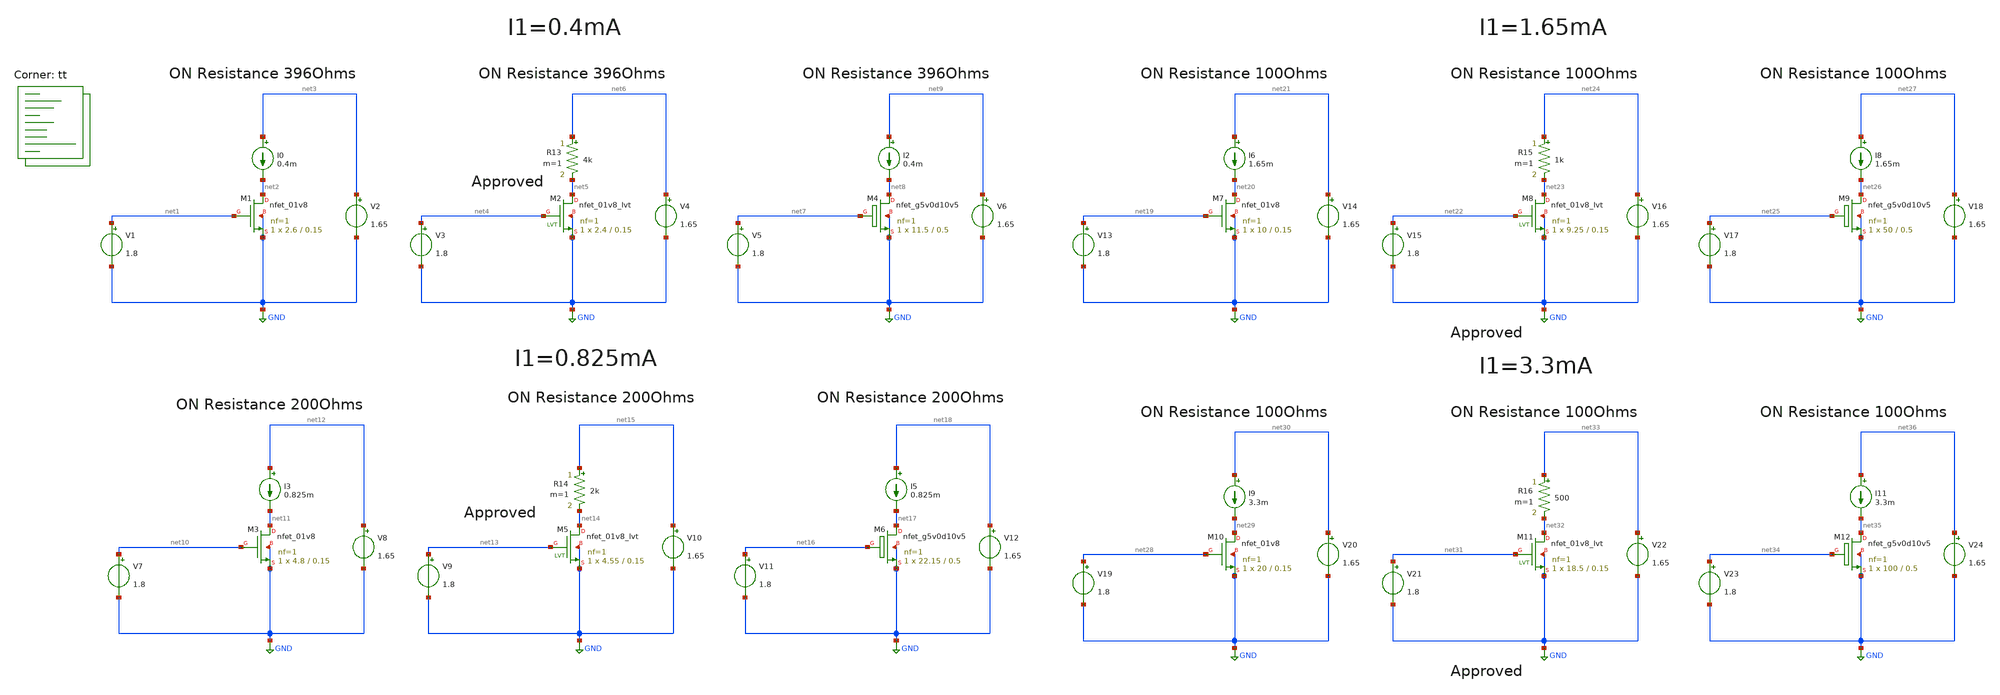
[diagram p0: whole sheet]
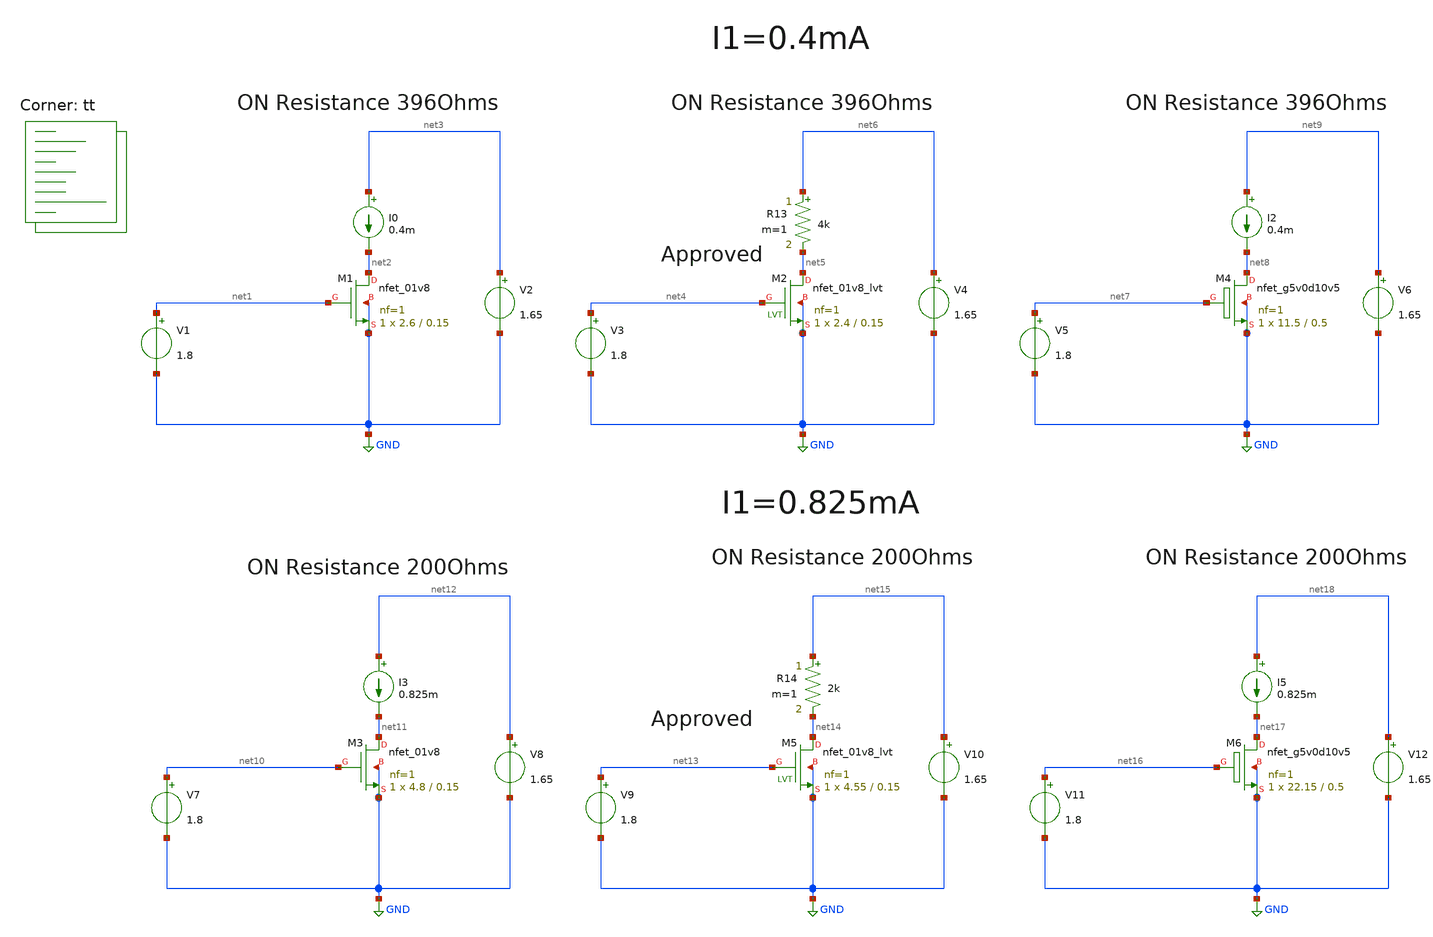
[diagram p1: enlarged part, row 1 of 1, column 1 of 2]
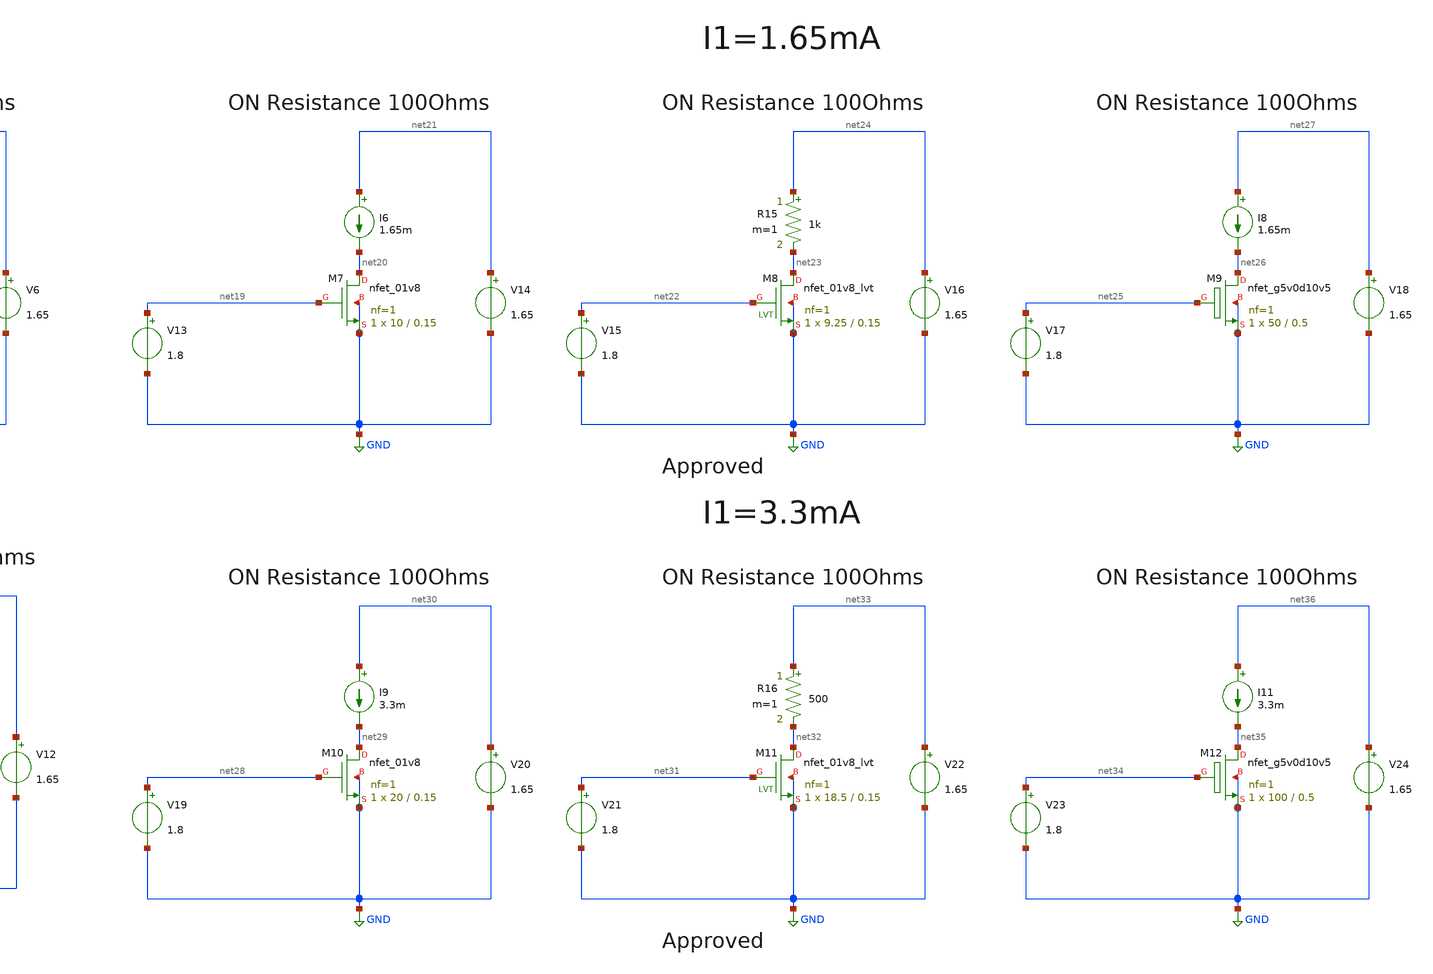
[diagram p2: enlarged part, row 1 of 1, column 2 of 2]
** sch_path: Switch-Res/Res1try.sch
**.subckt Res1try
V1 net1 GND 1.8
V2 net3 GND 1.65
I0 net3 net2 0.4m
XM1 net2 net1 GND GND sky130_fd_pr__nfet_01v8 L=0.15 W=2.6 nf=1 ad='int((nf+1)/2) * W/nf * 0.29' as='int((nf+2)/2) * W/nf * 0.29'
+ pd='2*int((nf+1)/2) * (W/nf + 0.29)' ps='2*int((nf+2)/2) * (W/nf + 0.29)' nrd='0.29 / W' nrs='0.29 / W'
+ sa=0 sb=0 sd=0 mult=1 m=1
V3 net4 GND 1.8
V4 net6 GND 1.65
XM2 net5 net4 GND GND sky130_fd_pr__nfet_01v8_lvt L=0.15 W=2.4 nf=1 ad='int((nf+1)/2) * W/nf * 0.29'
+ as='int((nf+2)/2) * W/nf * 0.29' pd='2*int((nf+1)/2) * (W/nf + 0.29)' ps='2*int((nf+2)/2) * (W/nf + 0.29)'
+ nrd='0.29 / W' nrs='0.29 / W' sa=0 sb=0 sd=0 mult=1 m=1
V5 net7 GND 1.8
V6 net9 GND 1.65
I2 net9 net8 0.4m
XM4 net8 net7 GND GND sky130_fd_pr__nfet_g5v0d10v5 L=0.5 W=11.5 nf=1 ad='int((nf+1)/2) * W/nf * 0.29'
+ as='int((nf+2)/2) * W/nf * 0.29' pd='2*int((nf+1)/2) * (W/nf + 0.29)' ps='2*int((nf+2)/2) * (W/nf + 0.29)'
+ nrd='0.29 / W' nrs='0.29 / W' sa=0 sb=0 sd=0 mult=1 m=1
V7 net10 GND 1.8
V8 net12 GND 1.65
I3 net12 net11 0.825m
XM3 net11 net10 GND GND sky130_fd_pr__nfet_01v8 L=0.15 W=4.8 nf=1 ad='int((nf+1)/2) * W/nf * 0.29' as='int((nf+2)/2) * W/nf * 0.29'
+ pd='2*int((nf+1)/2) * (W/nf + 0.29)' ps='2*int((nf+2)/2) * (W/nf + 0.29)' nrd='0.29 / W' nrs='0.29 / W'
+ sa=0 sb=0 sd=0 mult=1 m=1
V9 net13 GND 1.8
V10 net15 GND 1.65
XM5 net14 net13 GND GND sky130_fd_pr__nfet_01v8_lvt L=0.15 W=4.55 nf=1 ad='int((nf+1)/2) * W/nf * 0.29'
+ as='int((nf+2)/2) * W/nf * 0.29' pd='2*int((nf+1)/2) * (W/nf + 0.29)' ps='2*int((nf+2)/2) * (W/nf + 0.29)'
+ nrd='0.29 / W' nrs='0.29 / W' sa=0 sb=0 sd=0 mult=1 m=1
V11 net16 GND 1.8
V12 net18 GND 1.65
XM6 net17 net16 GND GND sky130_fd_pr__nfet_g5v0d10v5 L=0.5 W=22.15 nf=1 ad='int((nf+1)/2) * W/nf * 0.29'
+ as='int((nf+2)/2) * W/nf * 0.29' pd='2*int((nf+1)/2) * (W/nf + 0.29)' ps='2*int((nf+2)/2) * (W/nf + 0.29)'
+ nrd='0.29 / W' nrs='0.29 / W' sa=0 sb=0 sd=0 mult=1 m=1
I5 net18 net17 0.825m
V13 net19 GND 1.8
V14 net21 GND 1.65
I6 net21 net20 1.65m
XM7 net20 net19 GND GND sky130_fd_pr__nfet_01v8 L=0.15 W=10 nf=1 ad='int((nf+1)/2) * W/nf * 0.29' as='int((nf+2)/2) * W/nf * 0.29'
+ pd='2*int((nf+1)/2) * (W/nf + 0.29)' ps='2*int((nf+2)/2) * (W/nf + 0.29)' nrd='0.29 / W' nrs='0.29 / W'
+ sa=0 sb=0 sd=0 mult=1 m=1
V15 net22 GND 1.8
V16 net24 GND 1.65
XM8 net23 net22 GND GND sky130_fd_pr__nfet_01v8_lvt L=0.15 W=9.25 nf=1 ad='int((nf+1)/2) * W/nf * 0.29'
+ as='int((nf+2)/2) * W/nf * 0.29' pd='2*int((nf+1)/2) * (W/nf + 0.29)' ps='2*int((nf+2)/2) * (W/nf + 0.29)'
+ nrd='0.29 / W' nrs='0.29 / W' sa=0 sb=0 sd=0 mult=1 m=1
V17 net25 GND 1.8
V18 net27 GND 1.65
XM9 net26 net25 GND GND sky130_fd_pr__nfet_g5v0d10v5 L=0.5 W=50 nf=1 ad='int((nf+1)/2) * W/nf * 0.29'
+ as='int((nf+2)/2) * W/nf * 0.29' pd='2*int((nf+1)/2) * (W/nf + 0.29)' ps='2*int((nf+2)/2) * (W/nf + 0.29)'
+ nrd='0.29 / W' nrs='0.29 / W' sa=0 sb=0 sd=0 mult=1 m=1
I8 net27 net26 1.65m
V19 net28 GND 1.8
V20 net30 GND 1.65
I9 net30 net29 3.3m
XM10 net29 net28 GND GND sky130_fd_pr__nfet_01v8 L=0.15 W=20 nf=1 ad='int((nf+1)/2) * W/nf * 0.29' as='int((nf+2)/2) * W/nf * 0.29'
+ pd='2*int((nf+1)/2) * (W/nf + 0.29)' ps='2*int((nf+2)/2) * (W/nf + 0.29)' nrd='0.29 / W' nrs='0.29 / W'
+ sa=0 sb=0 sd=0 mult=1 m=1
V21 net31 GND 1.8
V22 net33 GND 1.65
XM11 net32 net31 GND GND sky130_fd_pr__nfet_01v8_lvt L=0.15 W=18.5 nf=1 ad='int((nf+1)/2) * W/nf * 0.29'
+ as='int((nf+2)/2) * W/nf * 0.29' pd='2*int((nf+1)/2) * (W/nf + 0.29)' ps='2*int((nf+2)/2) * (W/nf + 0.29)'
+ nrd='0.29 / W' nrs='0.29 / W' sa=0 sb=0 sd=0 mult=1 m=1
V23 net34 GND 1.8
V24 net36 GND 1.65
XM12 net35 net34 GND GND sky130_fd_pr__nfet_g5v0d10v5 L=0.5 W=100 nf=1 ad='int((nf+1)/2) * W/nf * 0.29'
+ as='int((nf+2)/2) * W/nf * 0.29' pd='2*int((nf+1)/2) * (W/nf + 0.29)' ps='2*int((nf+2)/2) * (W/nf + 0.29)'
+ nrd='0.29 / W' nrs='0.29 / W' sa=0 sb=0 sd=0 mult=1 m=1
I11 net36 net35 3.3m
R13 net6 net5 4k m=1
R14 net15 net14 2k m=1
R15 net24 net23 1k m=1
R16 net33 net32 500 m=1
**** begin user architecture code


.option wnflag=1
.option savecurrents
.temp 27
.control
save all
write Res1try.raw
set appendwrite
op
 show m : gm : gmbs : gds : vds : vdsat : vgs : vth : id: cgg
write Res1try.raw
tran 1m 10m 1m
.endc

.lib $::SKYWATER_MODELS/sky130.lib.spice tt
**** end user architecture code
**.ends
.GLOBAL GND
.end
